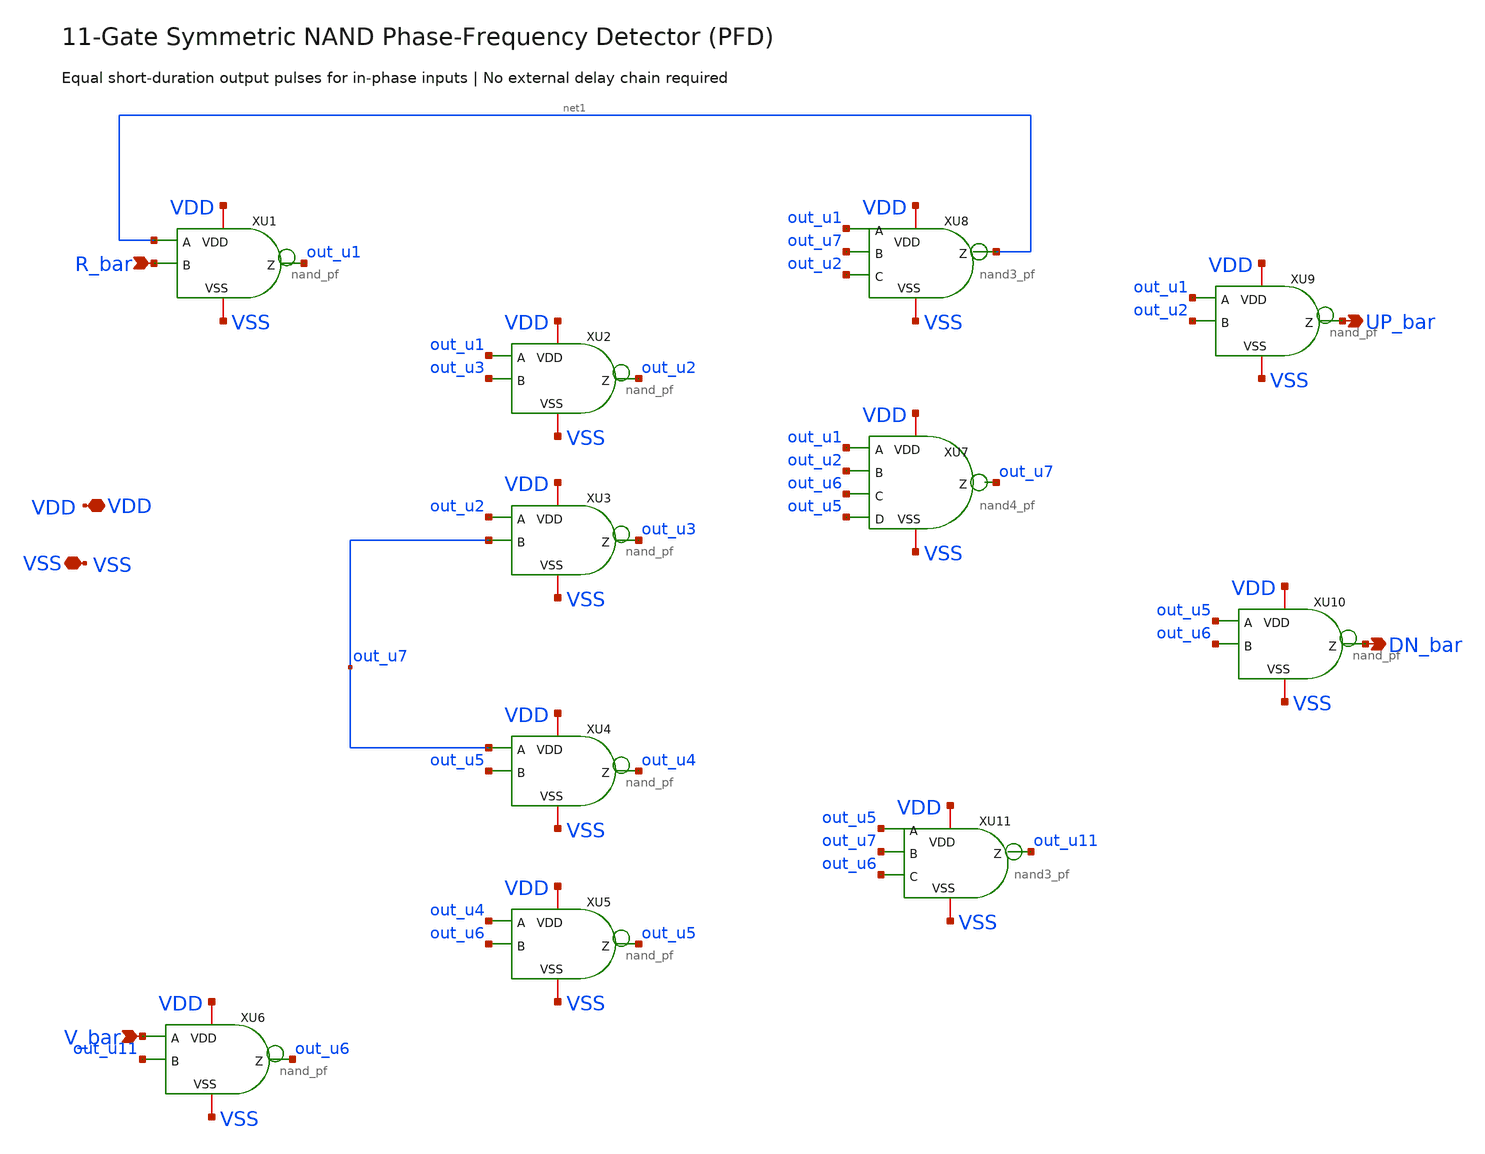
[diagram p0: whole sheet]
** sch_path: designs/libs/core_analog/pfd/pfd_11gate.sch
**.subckt pfd_11gate R_bar V_bar UP_bar DN_bar VDD VSS
*.ipin R_bar
*.ipin V_bar
*.opin UP_bar
*.opin DN_bar
*.iopin VDD
*.iopin VSS
XU1 VDD out_u1 net1 R_bar VSS nand_pf
XU2 VDD out_u2 out_u1 out_u3 VSS nand_pf
XU3 VDD out_u3 out_u2 out_u7 VSS nand_pf
XU4 VDD out_u4 out_u7 out_u5 VSS nand_pf
XU5 VDD out_u5 out_u4 out_u6 VSS nand_pf
XU6 VDD out_u6 V_bar out_u11 VSS nand_pf
XU7 VDD out_u7 out_u1 out_u2 out_u6 out_u5 VSS nand4_pf
XU8 VDD net1 out_u1 out_u7 out_u2 VSS nand3_pf
XU9 VDD UP_bar out_u1 out_u2 VSS nand_pf
XU10 VDD DN_bar out_u5 out_u6 VSS nand_pf
XU11 VDD out_u11 out_u5 out_u7 out_u6 VSS nand3_pf
**.ends
.end
